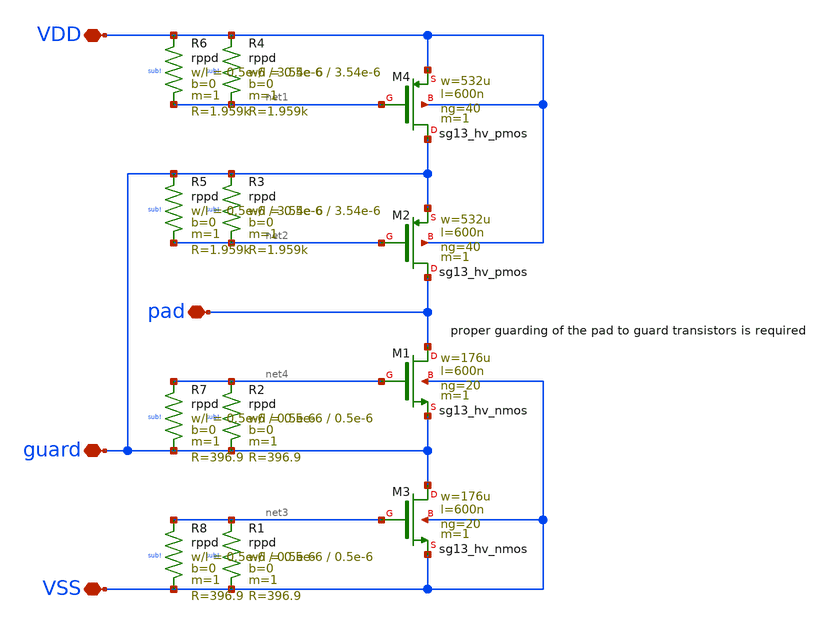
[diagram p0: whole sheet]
** sch_path: trident_test_structures/design_data/xschem/IOPadAnalogGuardLayer/clamps_guard_layer_x2.sch
**.subckt clamps_guard_layer_x2 VSS VDD pad guard
*.iopin VSS
*.iopin VDD
*.iopin pad
*.iopin guard
XM1 pad net4 guard VSS sg13_hv_nmos w=176u l=600n ng=20 m=1 mm_ok=1
XM3 guard net3 VSS VSS sg13_hv_nmos w=176u l=600n ng=20 m=1 mm_ok=1
XM2 pad net2 guard VDD sg13_hv_pmos w=532u l=600n ng=40 m=1 mm_ok=1
XR1 net3 VSS sub! rppd w=0.5e-6 l=0.5e-6 m=1 b=0 mm_ok=1
XR2 net4 guard sub! rppd w=0.5e-6 l=0.5e-6 m=1 b=0 mm_ok=1
XR3 guard net2 sub! rppd w=0.5e-6 l=3.54e-6 m=1 b=0 mm_ok=1
XR4 VDD net1 sub! rppd w=0.5e-6 l=3.54e-6 m=1 b=0 mm_ok=1
XM4 guard net1 VDD VDD sg13_hv_pmos w=532u l=600n ng=40 m=1 mm_ok=1
XR5 guard net2 sub! rppd w=0.5e-6 l=3.54e-6 m=1 b=0 mm_ok=1
XR6 VDD net1 sub! rppd w=0.5e-6 l=3.54e-6 m=1 b=0 mm_ok=1
XR7 net4 guard sub! rppd w=0.5e-6 l=0.5e-6 m=1 b=0 mm_ok=1
XR8 net3 VSS sub! rppd w=0.5e-6 l=0.5e-6 m=1 b=0 mm_ok=1
**.ends
.end
